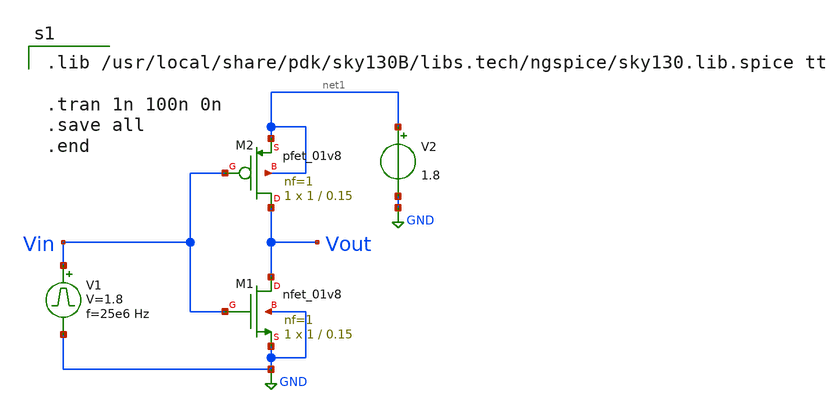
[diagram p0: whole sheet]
** sch_path: physical_design_layout_of_cmos_inverter/cmos_inverter.sch
**.subckt cmos_inverter
XM1 Vout Vin GND GND sky130_fd_pr__nfet_01v8 L=0.15 W=1 nf=1 ad='int((nf+1)/2) * W/nf * 0.29' as='int((nf+2)/2) * W/nf * 0.29'
+ pd='2*int((nf+1)/2) * (W/nf + 0.29)' ps='2*int((nf+2)/2) * (W/nf + 0.29)' nrd='0.29 / W' nrs='0.29 / W'
+ sa=0 sb=0 sd=0 mult=1 m=1
XM2 Vout Vin net1 net1 sky130_fd_pr__pfet_01v8 L=0.15 W=1 nf=1 ad='int((nf+1)/2) * W/nf * 0.29' as='int((nf+2)/2) * W/nf * 0.29'
+ pd='2*int((nf+1)/2) * (W/nf + 0.29)' ps='2*int((nf+2)/2) * (W/nf + 0.29)' nrd='0.29 / W' nrs='0.29 / W'
+ sa=0 sb=0 sd=0 mult=1 m=1
V1 Vin GND pulse 0 1.8 '0.495/ 25e6 ' '0.01/25e6 ' '0.01/25e6 ' '0.49/25e6 ' '1/25e6 '
V2 net1 GND 1.8
**** begin user architecture code

.lib /usr/local/share/pdk/sky130B/libs.tech/ngspice/sky130.lib.spice tt

.tran 1n 100n 0n
.save all
.end

**** end user architecture code
**.ends
.GLOBAL GND
.end
